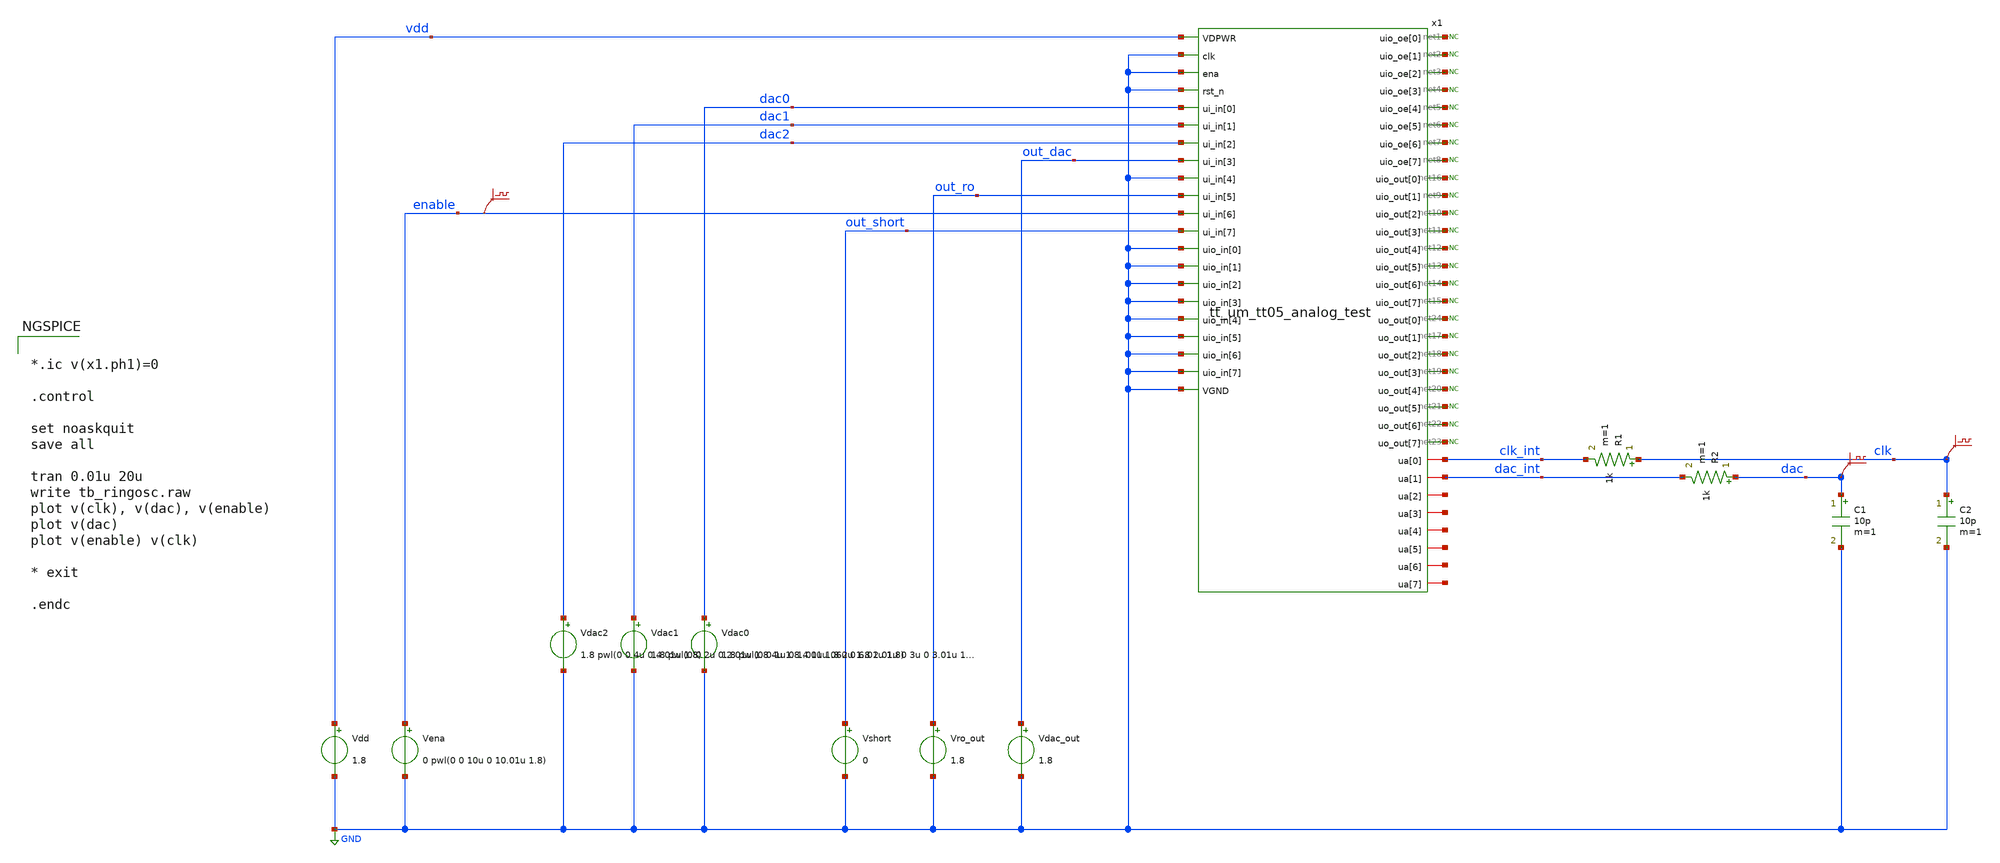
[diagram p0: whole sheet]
** sch_path: mag/Old design/xschem/tb_tt_um_tt05_analog_test.sch
**.subckt tb_tt_um_tt05_analog_test
Vdd vdd GND 1.8
C1 dac GND 10p m=1
C2 clk GND 10p m=1
.save v(clk)
.save v(dac)
R1 clk clk_int 1k m=1
R2 dac dac_int 1k m=1
Vena enable GND 0 pwl(0 0 10u 0 10.01u 1.8)
* noconn #net1
* noconn #net2
* noconn #net3
* noconn #net4
* noconn #net5
* noconn #net6
* noconn #net7
* noconn #net8
* noconn #net9
* noconn #net10
* noconn #net11
* noconn #net12
* noconn #net13
* noconn #net14
* noconn #net15
* noconn #net16
* noconn #net17
* noconn #net18
* noconn #net19
* noconn #net20
* noconn #net21
* noconn #net22
* noconn #net23
* noconn #net24
Vdac0 dac0 GND 1.8 pwl(0 0 1u 0 1.01u 1.8 2u 1.8 2.01u 0 3u 0 3.01u 1.8 4u 1.8 4.01u 0 5u 0 5.01u
+ 1.8 6u 1.8 6.01u 0 7u 0 7.01u 1.8)
Vdac1 dac1 GND 1.8 pwl(0 0 2u 0 2.01u 1.8 4u 1.8 4.01u 06u 0 6.01u 1.8)
Vdac2 dac2 GND 1.8 pwl(0 0 4u 0 4.01u 1.8)
.save v(enable)
Vshort out_short GND 0
Vro_out out_ro GND 1.8
Vdac_out out_dac GND 1.8
x1 net1 net2 net3 net4 net5 net6 net7 net8 vdd net16 net9 GND net10 GND GND net11 net12 net13 net14
+ dac0 dac1 net15 dac2 net24 out_dac net17 GND out_ro net18 enable net19 out_short net20 net21 GND net22
+ GND net23 GND GND clk_int GND dac_int GND net25 GND net26 GND net27 net28 net29 net30 GND
+ tt_um_tt05_analog_test
**** begin user architecture code

** opencircuitdesign pdks install
.lib $::SKYWATER_MODELS/sky130.lib.spice tt




*.ic v(x1.ph1)=0

.control

set noaskquit
save all

tran 0.01u 20u
write tb_ringosc.raw
plot v(clk), v(dac), v(enable)
plot v(dac)
plot v(enable) v(clk)

* exit

.endc


**** end user architecture code
**.ends
.GLOBAL GND
.end
